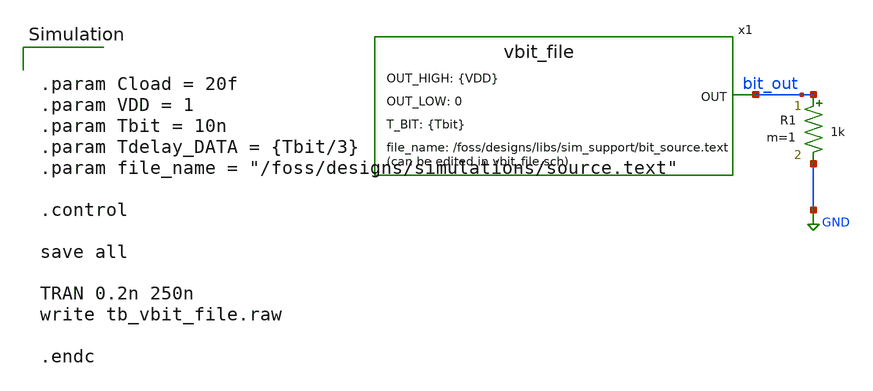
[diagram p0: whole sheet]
** sch_path: designs/libs/sim_support/tb_vbit_file_trial.sch
**.subckt tb_vbit_file_trial
R1 bit_out GND 1k m=1
x1 bit_out vbit_file T_BIT={Tbit} OUT_HIGH={VDD} OUT_LOW=0
**** begin user architecture code


.param Cload = 20f
.param VDD = 1
.param Tbit = 10n
.param Tdelay_DATA = {Tbit/3}
.param file_name = "/foss/designs/simulations/source.text"

.control

save all

TRAN 0.2n 250n
write tb_vbit_file.raw

.endc


**** end user architecture code
**.ends

* expanding   symbol:  sim_support/vbit_file.sym # of pins=1
** sym_path: designs/libs/sim_support/vbit_file.sym
** sch_path: designs/libs/sim_support/vbit_file.sch
.subckt vbit_file OUT  T_BIT=10n OUT_HIGH=3.3 OUT_LOW=0
*.opin OUT
A1 [ bit_d ] [ OUT ] dac_buff
**** begin user architecture code


asource [ bit_d ]  input_vector
.model input_vector d_source(input_file="/foss/designs/libs/sim_support/bit_source.text")


* Ain [ bit_node ] [ bit ] dac_in
.model dac_buff dac_bridge (out_low={OUT_LOW} out_high={OUT_HIGH} t_rise={T_BIT/10} t_fall={T_BIT/10})

**** end user architecture code
.ends

.GLOBAL GND
.end
